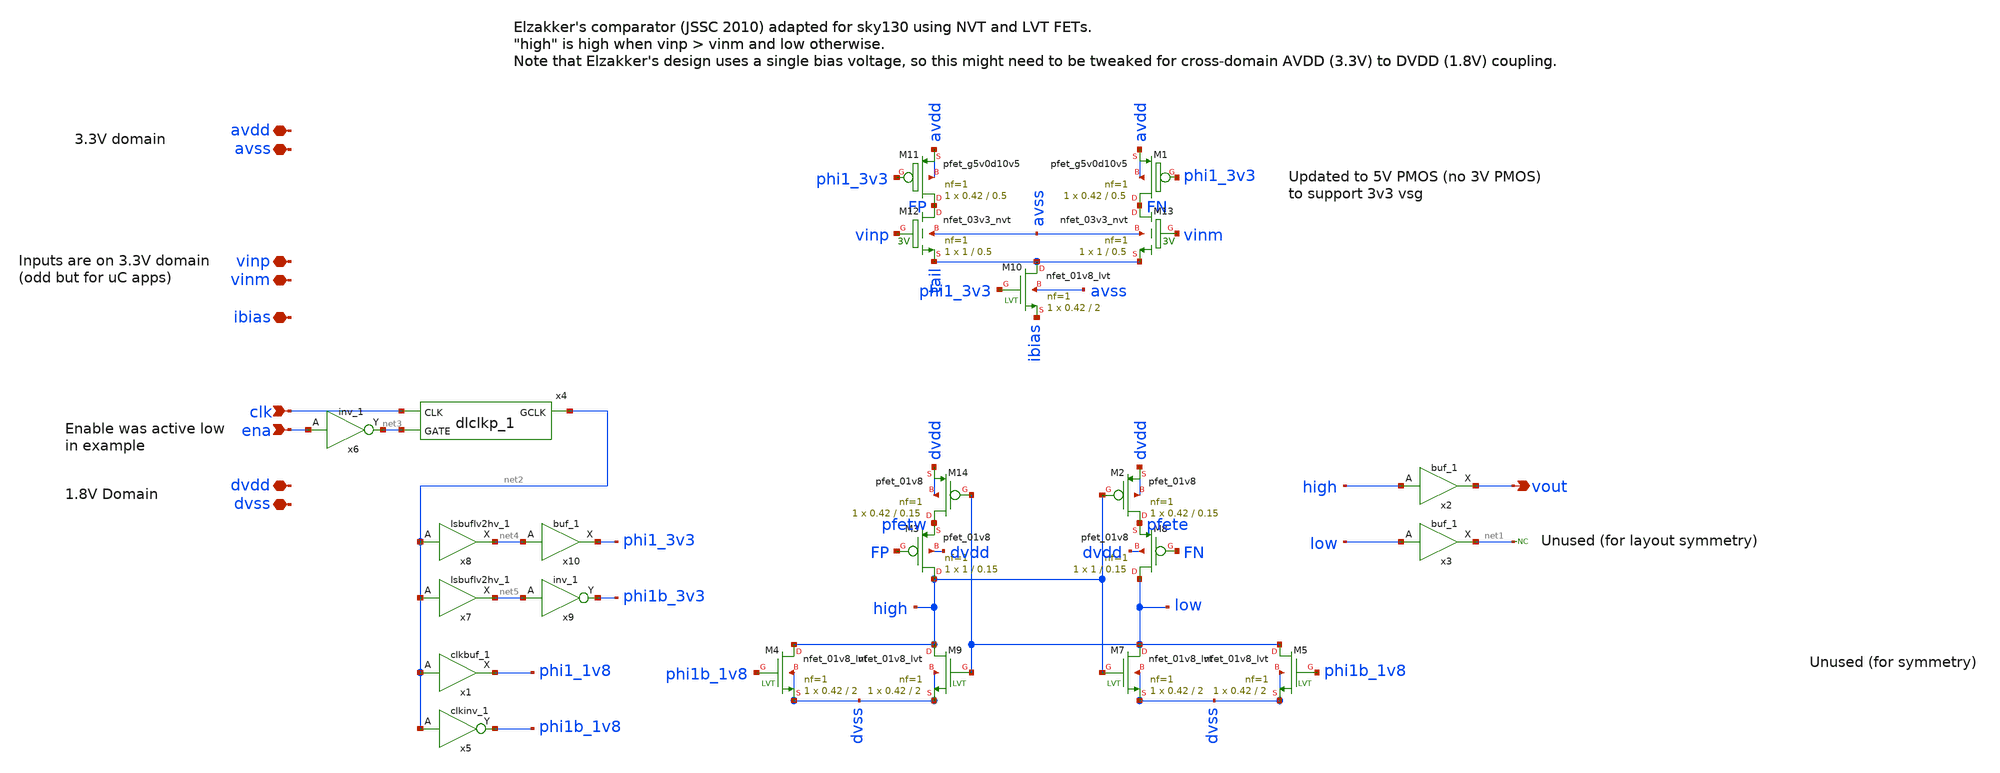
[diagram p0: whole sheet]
** sch_path: xschem/dynamic_comparator_hv2lv.sch
**.subckt dynamic_comparator_hv2lv clk vinp vinm dvdd dvss vout avdd avss ibias ena
*.ipin clk
*.iopin vinp
*.iopin vinm
*.iopin dvdd
*.iopin dvss
*.opin vout
*.iopin avdd
*.iopin avss
*.iopin ibias
*.ipin ena
XM12 FP vinp tail avss sky130_fd_pr__nfet_03v3_nvt L=0.5 W=1 nf=1 ad='int((nf+1)/2) * W/nf * 0.29' as='int((nf+2)/2) * W/nf * 0.29'
+ pd='2*int((nf+1)/2) * (W/nf + 0.29)' ps='2*int((nf+2)/2) * (W/nf + 0.29)' nrd='0.29 / W' nrs='0.29 / W'
+ sa=0 sb=0 sd=0 mult=1 m=1
XM13 FN vinm tail avss sky130_fd_pr__nfet_03v3_nvt L=0.5 W=1 nf=1 ad='int((nf+1)/2) * W/nf * 0.29' as='int((nf+2)/2) * W/nf * 0.29'
+ pd='2*int((nf+1)/2) * (W/nf + 0.29)' ps='2*int((nf+2)/2) * (W/nf + 0.29)' nrd='0.29 / W' nrs='0.29 / W'
+ sa=0 sb=0 sd=0 mult=1 m=1
XM14 pfetw low dvdd dvdd sky130_fd_pr__pfet_01v8 L=0.15 W=0.42 nf=1 ad='int((nf+1)/2) * W/nf * 0.29'
+ as='int((nf+2)/2) * W/nf * 0.29' pd='2*int((nf+1)/2) * (W/nf + 0.29)' ps='2*int((nf+2)/2) * (W/nf + 0.29)'
+ nrd='0.29 / W' nrs='0.29 / W' sa=0 sb=0 sd=0 mult=1 m=1
XM3 high FP pfetw dvdd sky130_fd_pr__pfet_01v8 L=0.15 W=1 nf=1 ad='int((nf+1)/2) * W/nf * 0.29' as='int((nf+2)/2) * W/nf * 0.29'
+ pd='2*int((nf+1)/2) * (W/nf + 0.29)' ps='2*int((nf+2)/2) * (W/nf + 0.29)' nrd='0.29 / W' nrs='0.29 / W'
+ sa=0 sb=0 sd=0 mult=1 m=1
XM8 low FN pfete dvdd sky130_fd_pr__pfet_01v8 L=0.15 W=1 nf=1 ad='int((nf+1)/2) * W/nf * 0.29' as='int((nf+2)/2) * W/nf * 0.29'
+ pd='2*int((nf+1)/2) * (W/nf + 0.29)' ps='2*int((nf+2)/2) * (W/nf + 0.29)' nrd='0.29 / W' nrs='0.29 / W'
+ sa=0 sb=0 sd=0 mult=1 m=1
XM2 pfete high dvdd dvdd sky130_fd_pr__pfet_01v8 L=0.15 W=0.42 nf=1 ad='int((nf+1)/2) * W/nf * 0.29'
+ as='int((nf+2)/2) * W/nf * 0.29' pd='2*int((nf+1)/2) * (W/nf + 0.29)' ps='2*int((nf+2)/2) * (W/nf + 0.29)'
+ nrd='0.29 / W' nrs='0.29 / W' sa=0 sb=0 sd=0 mult=1 m=1
XM7 low high dvss dvss sky130_fd_pr__nfet_01v8_lvt L=2 W=0.42 nf=1 ad='int((nf+1)/2) * W/nf * 0.29' as='int((nf+2)/2) * W/nf * 0.29'
+ pd='2*int((nf+1)/2) * (W/nf + 0.29)' ps='2*int((nf+2)/2) * (W/nf + 0.29)' nrd='0.29 / W' nrs='0.29 / W'
+ sa=0 sb=0 sd=0 mult=1 m=1
XM9 high low dvss dvss sky130_fd_pr__nfet_01v8_lvt L=2 W=0.42 nf=1 ad='int((nf+1)/2) * W/nf * 0.29' as='int((nf+2)/2) * W/nf * 0.29'
+ pd='2*int((nf+1)/2) * (W/nf + 0.29)' ps='2*int((nf+2)/2) * (W/nf + 0.29)' nrd='0.29 / W' nrs='0.29 / W'
+ sa=0 sb=0 sd=0 mult=1 m=1
XM10 tail phi1_3v3 ibias avss sky130_fd_pr__nfet_01v8_lvt L=2 W=0.42 nf=1 ad='int((nf+1)/2) * W/nf * 0.29'
+ as='int((nf+2)/2) * W/nf * 0.29' pd='2*int((nf+1)/2) * (W/nf + 0.29)' ps='2*int((nf+2)/2) * (W/nf + 0.29)'
+ nrd='0.29 / W' nrs='0.29 / W' sa=0 sb=0 sd=0 mult=1 m=1
XM4 high phi1b_1v8 dvss dvss sky130_fd_pr__nfet_01v8_lvt L=2 W=0.42 nf=1 ad='int((nf+1)/2) * W/nf * 0.29'
+ as='int((nf+2)/2) * W/nf * 0.29' pd='2*int((nf+1)/2) * (W/nf + 0.29)' ps='2*int((nf+2)/2) * (W/nf + 0.29)'
+ nrd='0.29 / W' nrs='0.29 / W' sa=0 sb=0 sd=0 mult=1 m=1
XM5 low phi1b_1v8 dvss dvss sky130_fd_pr__nfet_01v8_lvt L=2 W=0.42 nf=1 ad='int((nf+1)/2) * W/nf * 0.29'
+ as='int((nf+2)/2) * W/nf * 0.29' pd='2*int((nf+1)/2) * (W/nf + 0.29)' ps='2*int((nf+2)/2) * (W/nf + 0.29)'
+ nrd='0.29 / W' nrs='0.29 / W' sa=0 sb=0 sd=0 mult=1 m=1
x2 high dvss dvss dvdd dvdd vout sky130_fd_sc_hd__buf_1
x3 low dvss dvss dvdd dvdd net1 sky130_fd_sc_hd__buf_1
x4 clk net3 dvss dvss dvdd dvdd net2 sky130_fd_sc_hd__dlclkp_1
x1 net2 dvss dvss dvdd dvdd phi1_1v8 sky130_fd_sc_hd__clkbuf_1
x5 net2 dvss dvss dvdd dvdd phi1b_1v8 sky130_fd_sc_hd__clkinv_1
x6 ena dvss dvss dvdd dvdd net3 sky130_fd_sc_hd__inv_1
x7 net2 dvdd dvss dvss avdd avdd net5 sky130_fd_sc_hvl__lsbuflv2hv_1
x8 net2 dvdd dvss dvss avdd avdd net4 sky130_fd_sc_hvl__lsbuflv2hv_1
x9 net5 dvss dvss dvdd dvdd phi1b_3v3 sky130_fd_sc_hvl__inv_1
x10 net4 dvss dvss dvdd dvdd phi1_3v3 sky130_fd_sc_hvl__buf_1
* noconn #net1
XM11 FP phi1_3v3 avdd avdd sky130_fd_pr__pfet_g5v0d10v5 L=0.5 W=0.42 nf=1 ad='int((nf+1)/2) * W/nf * 0.29'
+ as='int((nf+2)/2) * W/nf * 0.29' pd='2*int((nf+1)/2) * (W/nf + 0.29)' ps='2*int((nf+2)/2) * (W/nf + 0.29)'
+ nrd='0.29 / W' nrs='0.29 / W' sa=0 sb=0 sd=0 mult=1 m=1
XM1 FN phi1_3v3 avdd avdd sky130_fd_pr__pfet_g5v0d10v5 L=0.5 W=0.42 nf=1 ad='int((nf+1)/2) * W/nf * 0.29'
+ as='int((nf+2)/2) * W/nf * 0.29' pd='2*int((nf+1)/2) * (W/nf + 0.29)' ps='2*int((nf+2)/2) * (W/nf + 0.29)'
+ nrd='0.29 / W' nrs='0.29 / W' sa=0 sb=0 sd=0 mult=1 m=1
**.ends
.end
